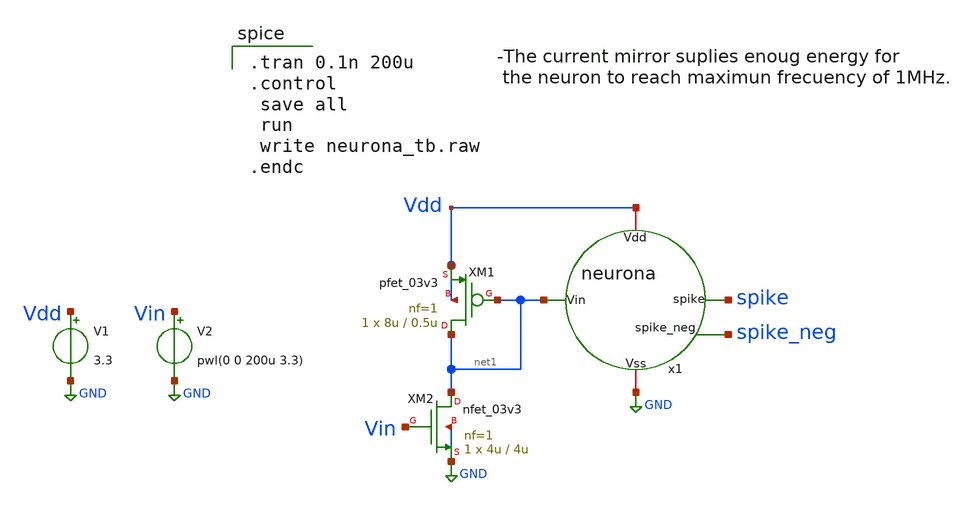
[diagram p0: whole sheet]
** sch_path: sch/lif/neurona_tb.sch
**.subckt neurona_tb
x1 Vdd GND net1 spike spike_neg neurona
V1 Vdd GND 3.3
V2 Vin GND pwl(0 0 200u 3.3)
XM1 net1 net1 Vdd Vdd pfet_03v3 L=0.5u W=8u nf=1 ad='int((nf+1)/2) * W/nf * 0.18u' as='int((nf+2)/2) * W/nf * 0.18u'
+ pd='2*int((nf+1)/2) * (W/nf + 0.18u)' ps='2*int((nf+2)/2) * (W/nf + 0.18u)' nrd='0.18u / W' nrs='0.18u / W'
+ sa=0 sb=0 sd=0 m=1
XM2 net1 Vin GND GND nfet_03v3 L=4u W=4u nf=1 ad='int((nf+1)/2) * W/nf * 0.18u' as='int((nf+2)/2) * W/nf * 0.18u'
+ pd='2*int((nf+1)/2) * (W/nf + 0.18u)' ps='2*int((nf+2)/2) * (W/nf + 0.18u)' nrd='0.18u / W' nrs='0.18u / W'
+ sa=0 sb=0 sd=0 m=1
**** begin user architecture code

.tran 0.1n 200u
.control
 save all
 run
 write neurona_tb.raw
.endc


.include $::180MCU_MODELS/design.ngspice
.lib $::180MCU_MODELS/sm141064.ngspice typical

**** end user architecture code
**.ends

* expanding   symbol:  CapiMagics/sch/lif/neurona.sym # of pins=5
** sym_path: CapiMagics/sch/lif/neurona.sym
** sch_path: CapiMagics/sch/lif/neurona.sch
.subckt neurona Vdd Vss Vin spike spike_neg
*.iopin Vdd
*.iopin Vss
*.ipin Vin
*.opin spike
*.opin spike_neg
XM1 spike_neg integration Vdd Vdd pfet_03v3 L=0.28u W=0.22u nf=1 ad='int((nf+1)/2) * W/nf * 0.18u' as='int((nf+2)/2) * W/nf * 0.18u'
+ pd='2*int((nf+1)/2) * (W/nf + 0.18u)' ps='2*int((nf+2)/2) * (W/nf + 0.18u)' nrd='0.18u / W' nrs='0.18u / W'
+ sa=0 sb=0 sd=0 m=1
XM2 spike_neg integration Vss Vss nfet_03v3 L=0.28u W=0.22u nf=1 ad='int((nf+1)/2) * W/nf * 0.18u' as='int((nf+2)/2) * W/nf * 0.18u'
+ pd='2*int((nf+1)/2) * (W/nf + 0.18u)' ps='2*int((nf+2)/2) * (W/nf + 0.18u)' nrd='0.18u / W' nrs='0.18u / W'
+ sa=0 sb=0 sd=0 m=1
XM3 spike/reset spike_neg Vdd Vdd pfet_03v3 L=0.28u W=0.22u nf=1 ad='int((nf+1)/2) * W/nf * 0.18u' as='int((nf+2)/2) * W/nf * 0.18u'
+ pd='2*int((nf+1)/2) * (W/nf + 0.18u)' ps='2*int((nf+2)/2) * (W/nf + 0.18u)' nrd='0.18u / W' nrs='0.18u / W'
+ sa=0 sb=0 sd=0 m=1
XM4 spike/reset spike_neg Vss Vss nfet_03v3 L=0.28u W=0.22u nf=1 ad='int((nf+1)/2) * W/nf * 0.18u' as='int((nf+2)/2) * W/nf * 0.18u'
+ pd='2*int((nf+1)/2) * (W/nf + 0.18u)' ps='2*int((nf+2)/2) * (W/nf + 0.18u)' nrd='0.18u / W' nrs='0.18u / W'
+ sa=0 sb=0 sd=0 m=1
XM7 spike spike_neg Vdd Vdd pfet_03v3 L=0.28u W=0.22u nf=1 ad='int((nf+1)/2) * W/nf * 0.18u' as='int((nf+2)/2) * W/nf * 0.18u'
+ pd='2*int((nf+1)/2) * (W/nf + 0.18u)' ps='2*int((nf+2)/2) * (W/nf + 0.18u)' nrd='0.18u / W' nrs='0.18u / W'
+ sa=0 sb=0 sd=0 m=1
XM8 spike spike_neg GND GND nfet_03v3 L=0.28u W=0.22u nf=1 ad='int((nf+1)/2) * W/nf * 0.18u' as='int((nf+2)/2) * W/nf * 0.18u'
+ pd='2*int((nf+1)/2) * (W/nf + 0.18u)' ps='2*int((nf+2)/2) * (W/nf + 0.18u)' nrd='0.18u / W' nrs='0.18u / W'
+ sa=0 sb=0 sd=0 m=1
XM5 integration spike/reset Vss Vss nfet_03v3 L=50u W=1.25u nf=1 ad='int((nf+1)/2) * W/nf * 0.18u' as='int((nf+2)/2) * W/nf * 0.18u'
+ pd='2*int((nf+1)/2) * (W/nf + 0.18u)' ps='2*int((nf+2)/2) * (W/nf + 0.18u)' nrd='0.18u / W' nrs='0.18u / W'
+ sa=0 sb=0 sd=0 m=1
C1 integration Vss 150f m=1
XM6 integration Vin Vdd Vdd pfet_03v3 L=17u W=0.22u nf=1 ad='int((nf+1)/2) * W/nf * 0.18u' as='int((nf+2)/2) * W/nf * 0.18u'
+ pd='2*int((nf+1)/2) * (W/nf + 0.18u)' ps='2*int((nf+2)/2) * (W/nf + 0.18u)' nrd='0.18u / W' nrs='0.18u / W'
+ sa=0 sb=0 sd=0 m=1
.ends

.GLOBAL GND
.end
